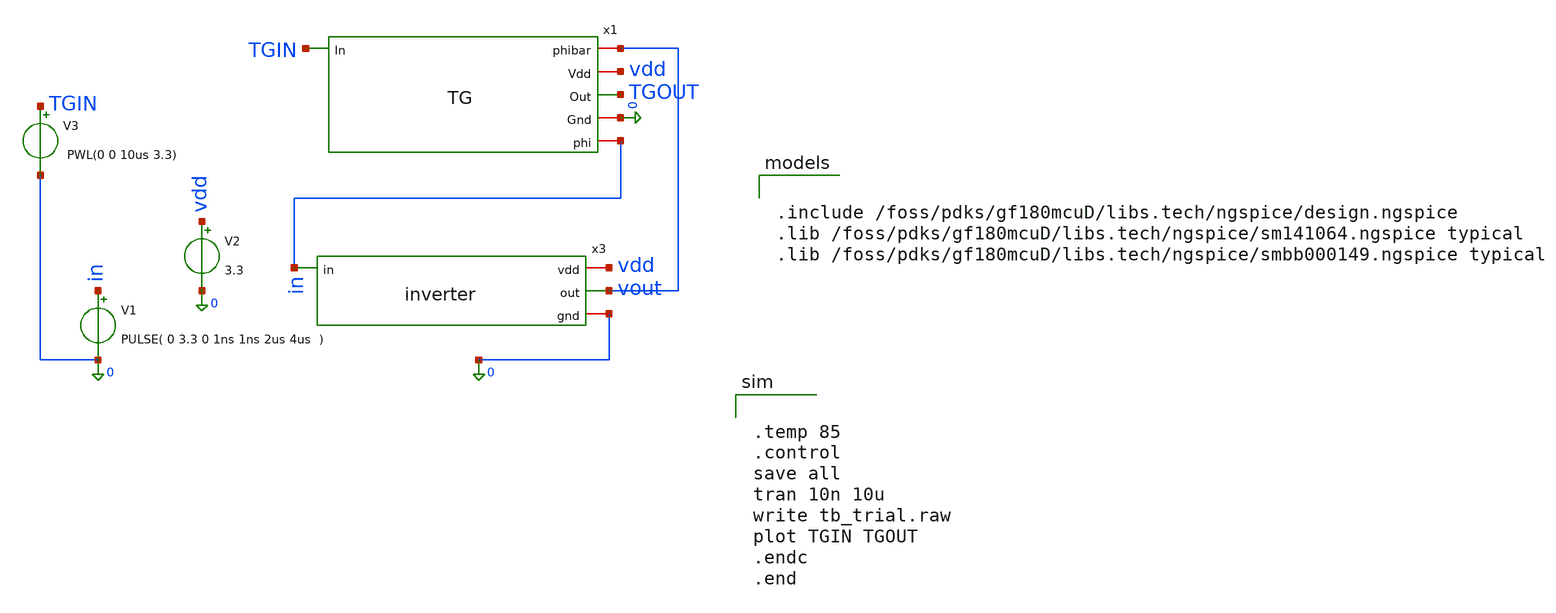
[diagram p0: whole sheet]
** sch_path: xschem/c2v_frontend/TG_testbench.sch
**.subckt TG_testbench
x1 vout vdd TGIN TGOUT 0 in TG
x3 vdd in vout 0 inverter
V1 in 0 PULSE( 0 3.3 0 1ns 1ns 2us 4us )
V2 vdd 0 3.3
V3 TGIN 0 PWL(0 0 10us 3.3)
**** begin user architecture code


.include /foss/pdks/gf180mcuD/libs.tech/ngspice/design.ngspice
.lib /foss/pdks/gf180mcuD/libs.tech/ngspice/sm141064.ngspice typical
.lib /foss/pdks/gf180mcuD/libs.tech/ngspice/smbb000149.ngspice typical




.temp 85
.control
save all
tran 10n 10u
write tb_trial.raw
plot TGIN TGOUT
.endc
.end


**** end user architecture code
**.ends

* expanding   symbol:  TG.sym # of pins=6
** sym_path: xschem/c2v_frontend/TG.sym
** sch_path: xschem/c2v_frontend/TG.sch
.subckt TG phibar Vdd In Out Gnd phi
*.ipin In
*.opin Out
*.iopin phi
*.iopin phibar
*.iopin Vdd
*.iopin Gnd
XM1 Out phi In Gnd nfet_03v3 L=0.34u W=2u nf=1 ad='int((nf+1)/2) * W/nf * 0.18u' as='int((nf+2)/2) * W/nf * 0.18u'
+ pd='2*int((nf+1)/2) * (W/nf + 0.18u)' ps='2*int((nf+2)/2) * (W/nf + 0.18u)' nrd='0.18u / W' nrs='0.18u / W'
+ sa=0 sb=0 sd=0 m=1
XM2 Out phibar In Vdd pfet_03v3 L=0.34u W=4u nf=1 ad='int((nf+1)/2) * W/nf * 0.18u' as='int((nf+2)/2) * W/nf * 0.18u'
+ pd='2*int((nf+1)/2) * (W/nf + 0.18u)' ps='2*int((nf+2)/2) * (W/nf + 0.18u)' nrd='0.18u / W' nrs='0.18u / W'
+ sa=0 sb=0 sd=0 m=1
.ends


* expanding   symbol:  inverter.sym # of pins=4
** sym_path: xschem/c2v_frontend/inverter.sym
** sch_path: xschem/c2v_frontend/inverter.sch
.subckt inverter vdd in out gnd
*.iopin vdd
*.iopin gnd
*.ipin in
*.opin out
XM1 out in vdd vdd pfet_03v3 L=1u W=5u nf=1 ad='int((nf+1)/2) * W/nf * 0.18u' as='int((nf+2)/2) * W/nf * 0.18u'
+ pd='2*int((nf+1)/2) * (W/nf + 0.18u)' ps='2*int((nf+2)/2) * (W/nf + 0.18u)' nrd='0.18u / W' nrs='0.18u / W'
+ sa=0 sb=0 sd=0 m=1
XM2 out in gnd gnd nfet_03v3 L=0.28u W=0.22u nf=1 ad='int((nf+1)/2) * W/nf * 0.18u' as='int((nf+2)/2) * W/nf * 0.18u'
+ pd='2*int((nf+1)/2) * (W/nf + 0.18u)' ps='2*int((nf+2)/2) * (W/nf + 0.18u)' nrd='0.18u / W' nrs='0.18u / W'
+ sa=0 sb=0 sd=0 m=1
.ends

.end
